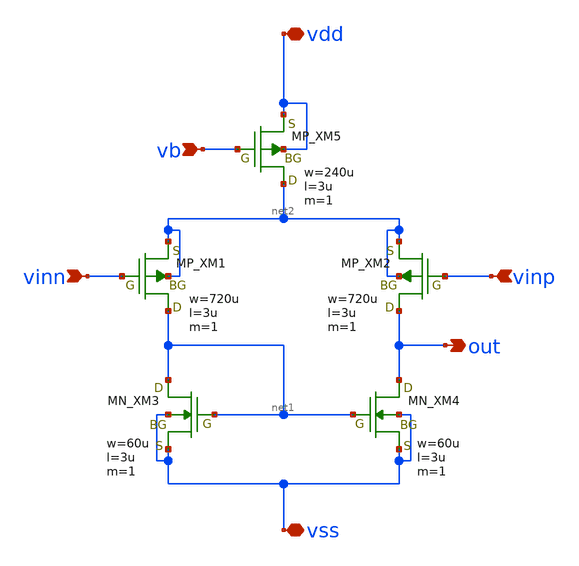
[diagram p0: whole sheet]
** sch_path: member_project/OPAMP/ShuntaroOhno/xschem/diff.sch
**.subckt diff vinn vinp vb out vdd vss
*.ipin vinn
*.ipin vinp
*.ipin vb
*.opin out
*.iopin vdd
*.iopin vss
XM5 net2 vb vdd vdd PMOS w=240u l=3u as=0 ad=0 ps=0 pd=0 nrd=0 nrs=0 m=1
XM1 net1 vinn net2 net2 PMOS w=720u l=3u as=0 ad=0 ps=0 pd=0 nrd=0 nrs=0 m=1
XM2 out vinp net2 net2 PMOS w=720u l=3u as=0 ad=0 ps=0 pd=0 nrd=0 nrs=0 m=1
XM3 net1 net1 vss vss NMOS w=60u l=3u as=0 ad=0 ps=0 pd=0 nrd=0 nrs=0 m=1
XM4 out net1 vss vss NMOS w=60u l=3u as=0 ad=0 ps=0 pd=0 nrd=0 nrs=0 m=1
**.ends
.end
